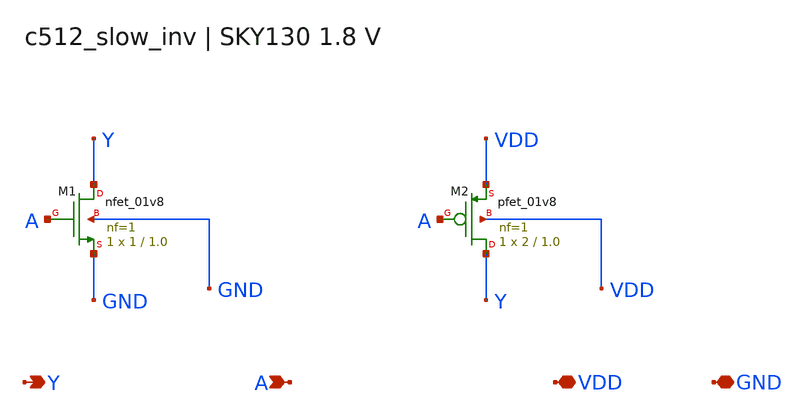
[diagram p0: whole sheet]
** sch_path: c512_slow_inv.sch
**.subckt c512_slow_inv Y A VDD GND
*.opin Y
*.ipin A
*.iopin VDD
*.iopin GND
XM1 Y A GND GND sky130_fd_pr__nfet_01v8 L=1.0 W=1 nf=1 ad=0.29 as=0.29 pd=2.58 ps=2.58 nrd=0.29
+ nrs=0.29 sa=0 sb=0 sd=0 mult=1 m=1
XM2 Y A VDD VDD sky130_fd_pr__pfet_01v8 L=1.0 W=2 nf=1 ad=0.58 as=0.58 pd=4.58 ps=4.58 nrd=0.145
+ nrs=0.145 sa=0 sb=0 sd=0 mult=1 m=1
**.ends
.end
